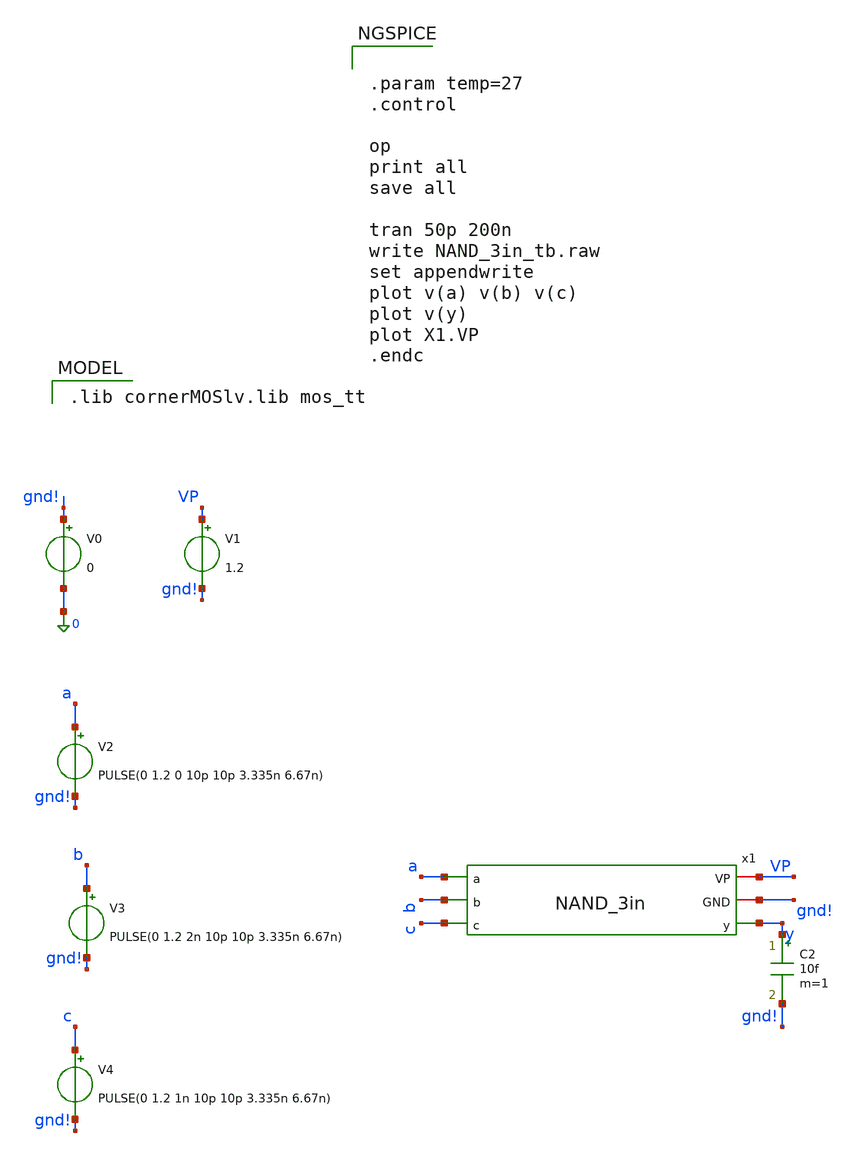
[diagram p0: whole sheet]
** sch_path: schematics/divider/NAND_3in_tb.sch
**.subckt NAND_3in_tb
x1 VP gnd! a y b c NAND_3in
V1 VP gnd! 1.2
V2 a gnd! PULSE(0 1.2 0 10p 10p 3.335n 6.67n)
V0 gnd! 0 0
C2 y gnd! 10f m=1
V3 b gnd! PULSE(0 1.2 2n 10p 10p 3.335n 6.67n)
V4 c gnd! PULSE(0 1.2 1n 10p 10p 3.335n 6.67n)
**** begin user architecture code
 .lib cornerMOSlv.lib mos_tt



.param temp=27
.control

op
print all
save all

tran 50p 200n
write NAND_3in_tb.raw
set appendwrite
plot v(a) v(b) v(c)
plot v(y)
plot X1.VP
.endc


**** end user architecture code
**.ends

* expanding   symbol:  /foss/designs/CHIP-PLL/divider/NAND_3in.sym # of pins=6
** sym_path: schematics/divider/schematics/NAND_3in.sym
** sch_path: schematics/divider/schematics/NAND_3in.sch
.subckt NAND_3in VP GND a y b c
*.opin y
*.iopin GND
*.ipin a
*.iopin VP
*.ipin b
*.ipin c
XM1 y a net2 GND sg13_lv_nmos w=0.15u l=0.13u ng=1 m=1 mm_ok=1
XM3 net2 b net1 GND sg13_lv_nmos w=0.15u l=0.13u ng=1 m=1 mm_ok=1
XM4 net1 c GND GND sg13_lv_nmos w=0.15u l=0.13u ng=1 m=1 mm_ok=1
XM7 y c VP VP sg13_lv_pmos w=0.15u l=0.13u ng=1 m=1 mm_ok=1
XM2 y a VP VP sg13_lv_pmos w=0.15u l=0.13u ng=1 m=1 mm_ok=1
XM5 y b VP VP sg13_lv_pmos w=0.15u l=0.13u ng=1 m=1 mm_ok=1
.ends

.end
